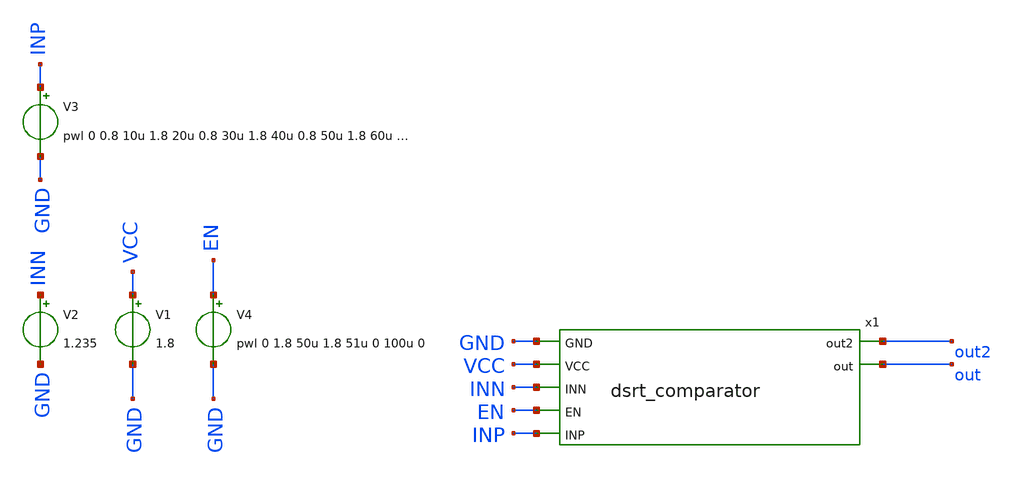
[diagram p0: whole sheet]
** sch_path: Kelompok7_Comparator/xsch/dsrt_comparator_sim.sch
**.subckt dsrt_comparator_sim
x1 GND VCC INN EN INP out2 out dsrt_comparator
V1 VCC GND 1.8
V2 INN GND 1.235
V3 INP GND pwl 0 0.8 10u 1.8 20u 0.8 30u 1.8 40u 0.8 50u 1.8 60u 0.8 70u 1.8 80u 0.8 90u 1.8 100u
+ 0.8
V4 EN GND pwl 0 1.8 50u 1.8 51u 0 100u 0
**** begin user architecture code
 .lib /foss/pdks/sky130A/libs.tech/ngspice/sky130.lib.spice tt

.param mc_mm_switch=0
.param mc_pr_switch=1



.option wnflag=0
.option savecurrents
.control
save all
*dc v2 0 1.8 0.01
*tran 10ps 30ns
tran 10n 100u
*plot inn inp out1 out2 out
plot inn inp out en
op
.endc


**** end user architecture code
**.ends

* expanding   symbol:  dsrt_comparator.sym # of pins=7
** sym_path: Kelompok7_Comparator/xsch/dsrt_comparator.sym
** sch_path: Kelompok7_Comparator/xsch/dsrt_comparator.sch
.subckt dsrt_comparator GND VCC INN EN INP out2 out
*.ipin VCC
*.ipin GND
*.ipin INP
*.ipin INN
*.ipin EN
*.opin out
*.opin out2
XM1 net3 INN net2 GND sky130_fd_pr__nfet_01v8 L=0.15 W=1 nf=1 ad='int((1 + 1)/2) * 1 / 1 * 0.29' as='int((1 + 2)/2) * 1 / 1 * 0.29'
+ pd='2*int((1 + 1)/2) * (1 / 1 + 0.29)' ps='2*int((1 + 2)/2) * (1 / 1 + 0.29)' nrd='0.29 / 1 ' nrs='0.29 / 1 '
+ sa=0 sb=0 sd=0 mult=1 m=1
XM2 net1 INP net2 GND sky130_fd_pr__nfet_01v8 L=0.15 W=1 nf=1 ad='int((1 + 1)/2) * 1 / 1 * 0.29' as='int((1 + 2)/2) * 1 / 1 * 0.29'
+ pd='2*int((1 + 1)/2) * (1 / 1 + 0.29)' ps='2*int((1 + 2)/2) * (1 / 1 + 0.29)' nrd='0.29 / 1 ' nrs='0.29 / 1 '
+ sa=0 sb=0 sd=0 mult=1 m=1
XM3 net1 net3 VCC VCC sky130_fd_pr__pfet_01v8 L=0.15 W=2 nf=1 ad='int((1 + 1)/2) * 2 / 1 * 0.29' as='int((1 + 2)/2) * 2 / 1 * 0.29'
+ pd='2*int((1 + 1)/2) * (2 / 1 + 0.29)' ps='2*int((1 + 2)/2) * (2 / 1 + 0.29)' nrd='0.29 / 2 ' nrs='0.29 / 2 '
+ sa=0 sb=0 sd=0 mult=1 m=1
XM4 net3 net3 VCC VCC sky130_fd_pr__pfet_01v8 L=0.15 W=2 nf=1 ad='int((1 + 1)/2) * 2 / 1 * 0.29' as='int((1 + 2)/2) * 2 / 1 * 0.29'
+ pd='2*int((1 + 1)/2) * (2 / 1 + 0.29)' ps='2*int((1 + 2)/2) * (2 / 1 + 0.29)' nrd='0.29 / 2 ' nrs='0.29 / 2 '
+ sa=0 sb=0 sd=0 mult=1 m=1
XM5 net2 VCC GND GND sky130_fd_pr__nfet_01v8 L=0.15 W=1 nf=1 ad='int((1 + 1)/2) * 1 / 1 * 0.29' as='int((1 + 2)/2) * 1 / 1 * 0.29'
+ pd='2*int((1 + 1)/2) * (1 / 1 + 0.29)' ps='2*int((1 + 2)/2) * (1 / 1 + 0.29)' nrd='0.29 / 1 ' nrs='0.29 / 1 '
+ sa=0 sb=0 sd=0 mult=1 m=1
**** begin user architecture code


.option wnflag=0
.option savecurrents
.control
save all
*dc v2 0 1.8 0.01
*tran 10ps 30ns
tran 10n 100u
*plot inn inp out1 out2 out
plot inn inp out en
op
.endc


**** end user architecture code
XM6 out1 net1 VCC VCC sky130_fd_pr__pfet_01v8 L=0.15 W=2 nf=1 ad='int((1 + 1)/2) * 2 / 1 * 0.29' as='int((1 + 2)/2) * 2 / 1 * 0.29'
+ pd='2*int((1 + 1)/2) * (2 / 1 + 0.29)' ps='2*int((1 + 2)/2) * (2 / 1 + 0.29)' nrd='0.29 / 2 ' nrs='0.29 / 2 '
+ sa=0 sb=0 sd=0 mult=1 m=1
XM7 out1 net1 GND GND sky130_fd_pr__nfet_01v8 L=0.15 W=1 nf=1 ad='int((1 + 1)/2) * 1 / 1 * 0.29' as='int((1 + 2)/2) * 1 / 1 * 0.29'
+ pd='2*int((1 + 1)/2) * (1 / 1 + 0.29)' ps='2*int((1 + 2)/2) * (1 / 1 + 0.29)' nrd='0.29 / 1 ' nrs='0.29 / 1 '
+ sa=0 sb=0 sd=0 mult=1 m=1
XM8 out2 out1 VCC VCC sky130_fd_pr__pfet_01v8 L=0.15 W=2 nf=1 ad='int((1 + 1)/2) * 2 / 1 * 0.29' as='int((1 + 2)/2) * 2 / 1 * 0.29'
+ pd='2*int((1 + 1)/2) * (2 / 1 + 0.29)' ps='2*int((1 + 2)/2) * (2 / 1 + 0.29)' nrd='0.29 / 2 ' nrs='0.29 / 2 '
+ sa=0 sb=0 sd=0 mult=1 m=1
XM9 out2 out1 net4 GND sky130_fd_pr__nfet_01v8 L=0.15 W=1 nf=1 ad='int((1 + 1)/2) * 1 / 1 * 0.29' as='int((1 + 2)/2) * 1 / 1 * 0.29'
+ pd='2*int((1 + 1)/2) * (1 / 1 + 0.29)' ps='2*int((1 + 2)/2) * (1 / 1 + 0.29)' nrd='0.29 / 1 ' nrs='0.29 / 1 '
+ sa=0 sb=0 sd=0 mult=1 m=1
XM10 out out2 VCC VCC sky130_fd_pr__pfet_01v8 L=0.15 W=2 nf=1 ad='int((1 + 1)/2) * 2 / 1 * 0.29' as='int((1 + 2)/2) * 2 / 1 * 0.29'
+ pd='2*int((1 + 1)/2) * (2 / 1 + 0.29)' ps='2*int((1 + 2)/2) * (2 / 1 + 0.29)' nrd='0.29 / 2 ' nrs='0.29 / 2 '
+ sa=0 sb=0 sd=0 mult=1 m=1
XM11 out out2 GND GND sky130_fd_pr__nfet_01v8 L=0.15 W=1 nf=1 ad='int((1 + 1)/2) * 1 / 1 * 0.29' as='int((1 + 2)/2) * 1 / 1 * 0.29'
+ pd='2*int((1 + 1)/2) * (1 / 1 + 0.29)' ps='2*int((1 + 2)/2) * (1 / 1 + 0.29)' nrd='0.29 / 1 ' nrs='0.29 / 1 '
+ sa=0 sb=0 sd=0 mult=1 m=1
XM13 net4 EN GND GND sky130_fd_pr__nfet_01v8 L=0.15 W=1 nf=1 ad='int((1 + 1)/2) * 1 / 1 * 0.29' as='int((1 + 2)/2) * 1 / 1 * 0.29'
+ pd='2*int((1 + 1)/2) * (1 / 1 + 0.29)' ps='2*int((1 + 2)/2) * (1 / 1 + 0.29)' nrd='0.29 / 1 ' nrs='0.29 / 1 '
+ sa=0 sb=0 sd=0 mult=1 m=1
XM12 out2 EN VCC VCC sky130_fd_pr__pfet_01v8 L=0.15 W=2 nf=1 ad='int((1 + 1)/2) * 2 / 1 * 0.29' as='int((1 + 2)/2) * 2 / 1 * 0.29'
+ pd='2*int((1 + 1)/2) * (2 / 1 + 0.29)' ps='2*int((1 + 2)/2) * (2 / 1 + 0.29)' nrd='0.29 / 2 ' nrs='0.29 / 2 '
+ sa=0 sb=0 sd=0 mult=1 m=1
.ends

.end
